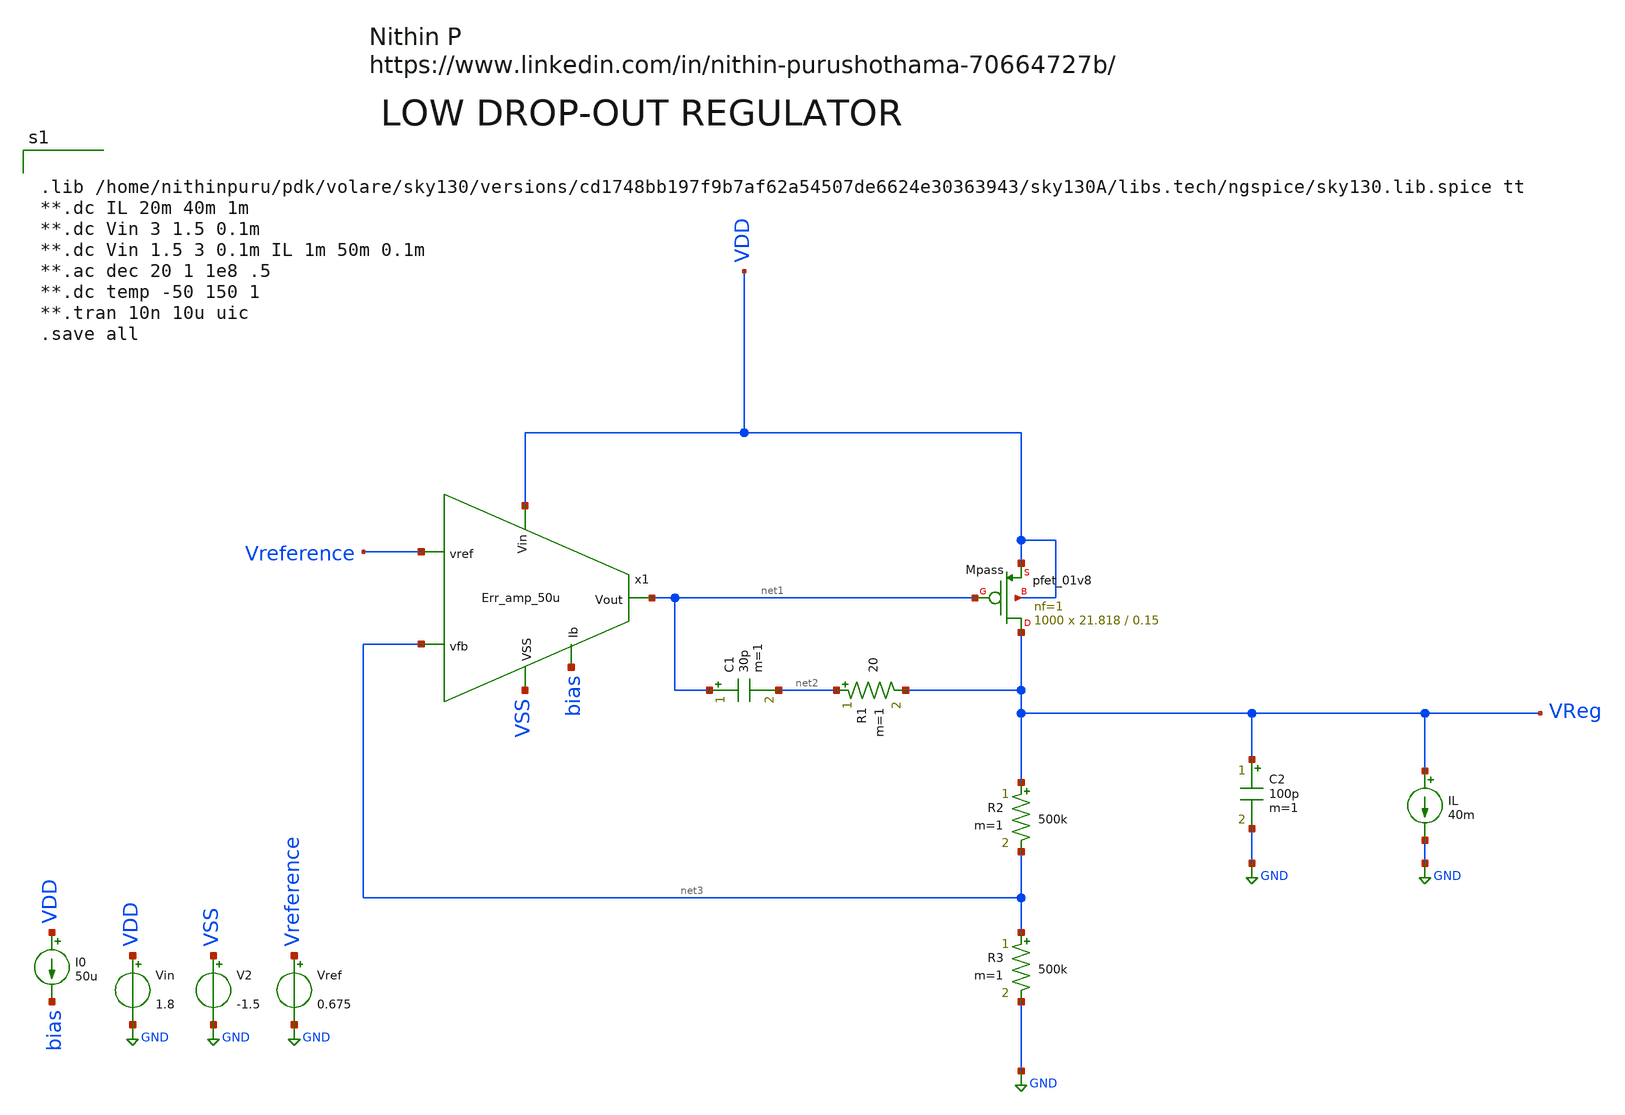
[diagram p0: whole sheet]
** sch_path: Schematics/Regulator.sch
**.subckt Regulator
x1 VDD VSS net3 net1 Vreference bias Err_amp_50u
Vin VDD GND 1.8
V2 VSS GND -1.5
Vref Vreference GND 0.675
I0 VDD bias 50u
C1 net1 net2 30p m=1
R1 net2 VReg 20 m=1
R2 VReg net3 500k m=1
R3 net3 GND 500k m=1
C2 VReg GND 100p m=1
XMpass VReg net1 VDD VDD sky130_fd_pr__pfet_01v8 L=0.15 W=21.818 nf=1 ad='int((nf+1)/2) * W/nf * 0.29'
+ as='int((nf+2)/2) * W/nf * 0.29' pd='2*int((nf+1)/2) * (W/nf + 0.29)' ps='2*int((nf+2)/2) * (W/nf + 0.29)'
+ nrd='0.29 / W' nrs='0.29 / W' sa=0 sb=0 sd=0 mult=1000 m=1000
IL VReg GND 40m
**** begin user architecture code


.lib /home/nithinpuru/pdk/volare/sky130/versions/cd1748bb197f9b7af62a54507de6624e30363943/sky130A/libs.tech/ngspice/sky130.lib.spice tt
**.dc IL 20m 40m 1m
**.dc Vin 3 1.5 0.1m
**.dc Vin 1.5 3 0.1m IL 1m 50m 0.1m
**.ac dec 20 1 1e8 .5
**.dc temp -50 150 1
**.tran 10n 10u uic
.save all

**** end user architecture code
**.ends

* expanding   symbol:  /home/nithinpuru/.xschem/simulations/Low drop regulator
*+ Project/Error_amplifier/Err_amp_50u.sym # of pins=6
** sym_path: Schematics/Err_amp_50u.sym
** sch_path: Schematics/Err_amp_50u.sch
.subckt Err_amp_50u Vin VSS vfb Vout vref Ib
*.ipin Vin
*.ipin VSS
*.ipin Ib
*.opin Vout
*.ipin vfb
*.ipin vref
XM36 net1 net1 Vin Vin sky130_fd_pr__pfet_01v8_lvt L=1 W=7 nf=1 ad='int((nf+1)/2) * W/nf * 0.29' as='int((nf+2)/2) * W/nf * 0.29'
+ pd='2*int((nf+1)/2) * (W/nf + 0.29)' ps='2*int((nf+2)/2) * (W/nf + 0.29)' nrd='0.29 / W' nrs='0.29 / W'
+ sa=0 sb=0 sd=0 mult=1 m=1
XM1 Vout net1 Vin Vin sky130_fd_pr__pfet_01v8_lvt L=1 W=7 nf=1 ad='int((nf+1)/2) * W/nf * 0.29' as='int((nf+2)/2) * W/nf * 0.29'
+ pd='2*int((nf+1)/2) * (W/nf + 0.29)' ps='2*int((nf+2)/2) * (W/nf + 0.29)' nrd='0.29 / W' nrs='0.29 / W'
+ sa=0 sb=0 sd=0 mult=1 m=1
XM31 net1 vfb net2 VSS sky130_fd_pr__nfet_01v8_lvt L=1 W=20.7 nf=1 ad='int((nf+1)/2) * W/nf * 0.29' as='int((nf+2)/2) * W/nf * 0.29'
+ pd='2*int((nf+1)/2) * (W/nf + 0.29)' ps='2*int((nf+2)/2) * (W/nf + 0.29)' nrd='0.29 / W' nrs='0.29 / W'
+ sa=0 sb=0 sd=0 mult=10 m=10
XM2 Vout vref net2 VSS sky130_fd_pr__nfet_01v8_lvt L=1 W=20.7 nf=1 ad='int((nf+1)/2) * W/nf * 0.29' as='int((nf+2)/2) * W/nf * 0.29'
+ pd='2*int((nf+1)/2) * (W/nf + 0.29)' ps='2*int((nf+2)/2) * (W/nf + 0.29)' nrd='0.29 / W' nrs='0.29 / W'
+ sa=0 sb=0 sd=0 mult=10 m=10
XM34 Ib Ib VSS VSS sky130_fd_pr__nfet_01v8_lvt L=1 W=5 nf=1 ad='int((nf+1)/2) * W/nf * 0.29' as='int((nf+2)/2) * W/nf * 0.29'
+ pd='2*int((nf+1)/2) * (W/nf + 0.29)' ps='2*int((nf+2)/2) * (W/nf + 0.29)' nrd='0.29 / W' nrs='0.29 / W'
+ sa=0 sb=0 sd=0 mult=1 m=1
XM3 net2 Ib VSS VSS sky130_fd_pr__nfet_01v8_lvt L=1 W=5 nf=1 ad='int((nf+1)/2) * W/nf * 0.29' as='int((nf+2)/2) * W/nf * 0.29'
+ pd='2*int((nf+1)/2) * (W/nf + 0.29)' ps='2*int((nf+2)/2) * (W/nf + 0.29)' nrd='0.29 / W' nrs='0.29 / W'
+ sa=0 sb=0 sd=0 mult=1 m=1
.ends

.GLOBAL GND
.end
